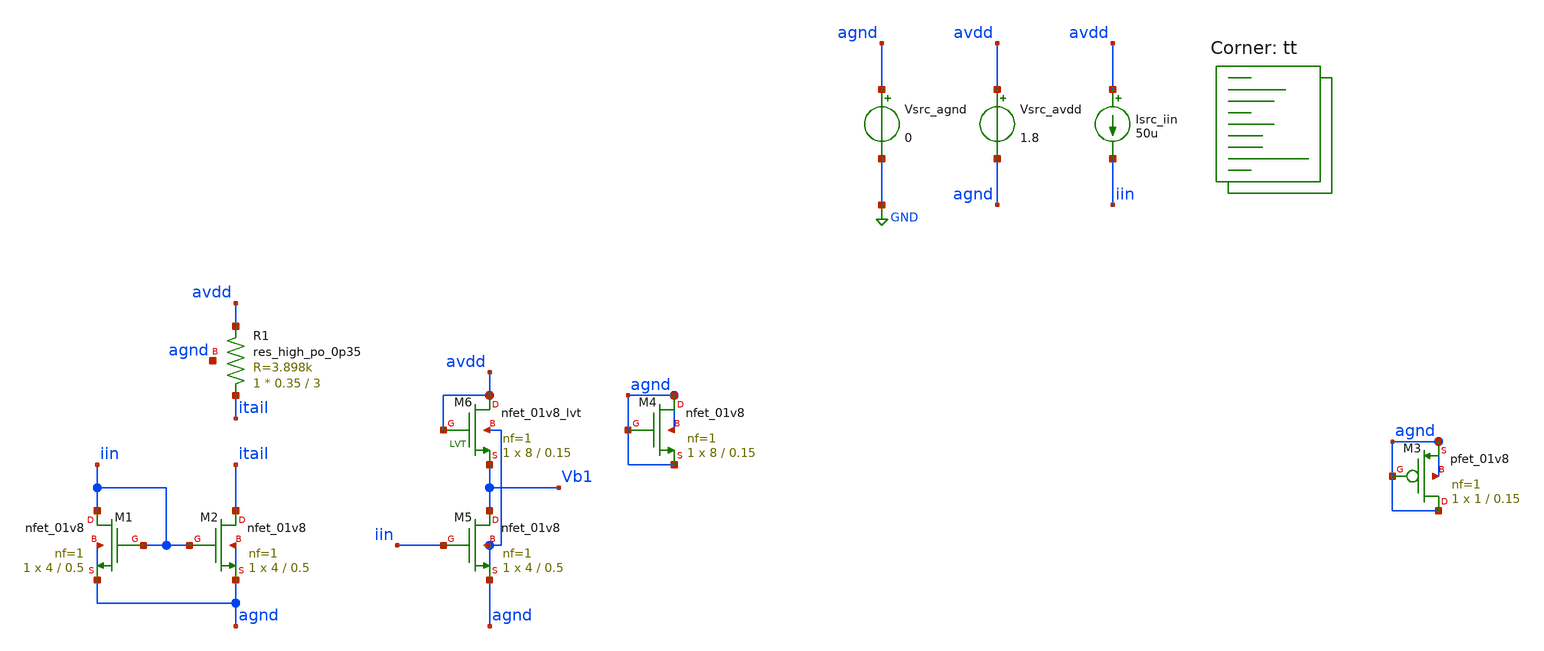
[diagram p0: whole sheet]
** sch_path: AMP/TB_Biases.sch
**.subckt TB_Biases
Vsrc_agnd agnd GND 0
Vsrc_avdd avdd agnd 1.8
Isrc_iin avdd iin 50u
XM1 iin iin agnd agnd sky130_fd_pr__nfet_01v8 L=0.5 W=4 nf=1 ad='int((nf+1)/2) * W/nf * 0.29' as='int((nf+2)/2) * W/nf * 0.29'
+ pd='2*int((nf+1)/2) * (W/nf + 0.29)' ps='2*int((nf+2)/2) * (W/nf + 0.29)' nrd='0.29 / W' nrs='0.29 / W'
+ sa=0 sb=0 sd=0 mult=1 m=1
XM2 itail iin agnd agnd sky130_fd_pr__nfet_01v8 L=0.5 W=4 nf=1 ad='int((nf+1)/2) * W/nf * 0.29' as='int((nf+2)/2) * W/nf * 0.29'
+ pd='2*int((nf+1)/2) * (W/nf + 0.29)' ps='2*int((nf+2)/2) * (W/nf + 0.29)' nrd='0.29 / W' nrs='0.29 / W'
+ sa=0 sb=0 sd=0 mult=1 m=1
XR1 itail avdd agnd sky130_fd_pr__res_high_po_0p35 L=3 mult=1 m=1
XM3 agnd agnd agnd agnd sky130_fd_pr__pfet_01v8 L=0.15 W=1 nf=1 ad='int((nf+1)/2) * W/nf * 0.29' as='int((nf+2)/2) * W/nf * 0.29'
+ pd='2*int((nf+1)/2) * (W/nf + 0.29)' ps='2*int((nf+2)/2) * (W/nf + 0.29)' nrd='0.29 / W' nrs='0.29 / W'
+ sa=0 sb=0 sd=0 mult=1 m=1
XM4 agnd agnd agnd agnd sky130_fd_pr__nfet_01v8 L=0.15 W=8 nf=1 ad='int((nf+1)/2) * W/nf * 0.29' as='int((nf+2)/2) * W/nf * 0.29'
+ pd='2*int((nf+1)/2) * (W/nf + 0.29)' ps='2*int((nf+2)/2) * (W/nf + 0.29)' nrd='0.29 / W' nrs='0.29 / W'
+ sa=0 sb=0 sd=0 mult=1 m=1
XM5 Vb1 iin agnd agnd sky130_fd_pr__nfet_01v8 L=0.5 W=4 nf=1 ad='int((nf+1)/2) * W/nf * 0.29' as='int((nf+2)/2) * W/nf * 0.29'
+ pd='2*int((nf+1)/2) * (W/nf + 0.29)' ps='2*int((nf+2)/2) * (W/nf + 0.29)' nrd='0.29 / W' nrs='0.29 / W'
+ sa=0 sb=0 sd=0 mult=1 m=1
XM6 avdd avdd Vb1 agnd sky130_fd_pr__nfet_01v8_lvt L=0.15 W=8 nf=1 ad='int((nf+1)/2) * W/nf * 0.29' as='int((nf+2)/2) * W/nf * 0.29'
+ pd='2*int((nf+1)/2) * (W/nf + 0.29)' ps='2*int((nf+2)/2) * (W/nf + 0.29)' nrd='0.29 / W' nrs='0.29 / W'
+ sa=0 sb=0 sd=0 mult=1 m=1
**** begin user architecture code

* this option enables mos model bin
* selection based on W/NF instead of W

.option savecurrents

.control
save all
op

* Print newline
echo

* Print stats for each MOSFET
foreach nmos xm1 xm2 xm4 xm5
 * Save stats
 save @m.{$nmos}.msky130_fd_pr__nfet_01v8[gm]
 let vth   = @m.{$nmos}.msky130_fd_pr__nfet_01v8[vth]
 let vgs   = @m.{$nmos}.msky130_fd_pr__nfet_01v8[vgs]
 let vds   = @m.{$nmos}.msky130_fd_pr__nfet_01v8[vds]
 let vdsat = @m.{$nmos}.msky130_fd_pr__nfet_01v8[vdsat]
 let gm    = @m.{$nmos}.msky130_fd_pr__nfet_01v8[gm]
 let gds   = @m.{$nmos}.msky130_fd_pr__nfet_01v8[gds]


 * Print stats
 echo Stats for $nmos:
 print vth
 print vgs
 print vds
 print vdsat
 print gm
 print gds

 * Print newline
 echo
end

foreach nmos_lvt xm6
 * Save stats
 save @m.{$nmos_lvt}.msky130_fd_pr__nfet_01v8_lvt[gm]
 let vth   = @m.{$nmos_lvt}.msky130_fd_pr__nfet_01v8_lvt[vth]
 let vgs   = @m.{$nmos_lvt}.msky130_fd_pr__nfet_01v8_lvt[vgs]
 let vds   = @m.{$nmos_lvt}.msky130_fd_pr__nfet_01v8_lvt[vds]
 let vdsat = @m.{$nmos_lvt}.msky130_fd_pr__nfet_01v8_lvt[vdsat]
 let gm    = @m.{$nmos_lvt}.msky130_fd_pr__nfet_01v8_lvt[gm]
 let gds   = @m.{$nmos_lvt}.msky130_fd_pr__nfet_01v8_lvt[gds]


 * Print stats
 echo Stats for $nmos_lvt:
 print vth
 print vgs
 print vds
 print vdsat
 print gm
 print gds

 * Print newline
 echo
end

foreach pmos xm3
 * Save stats
 save @m.{$pmos}.msky130_fd_pr__nfet_01v8[gm]
 let vth   = @m.{$pmos}.msky130_fd_pr__pfet_01v8[vth]
 let vgs   = @m.{$pmos}.msky130_fd_pr__pfet_01v8[vgs]
 let vds   = @m.{$pmos}.msky130_fd_pr__pfet_01v8[vds]
 let vdsat = @m.{$pmos}.msky130_fd_pr__pfet_01v8[vdsat]
 let gm    = @m.{$pmos}.msky130_fd_pr__pfet_01v8[gm]
 let gds   = @m.{$pmos}.msky130_fd_pr__pfet_01v8[gds]

 * Print stats
 echo Stats for $pmos:
 print vth
 print vgs
 print vds
 print vdsat
 print gm
 print gds

 * Print newline
 echo
end

* Print region of operation
echo Regions of Operation:
foreach nmos xm1 xm2 xm4 xm5
 * Save stats
 let vds = @m.{$nmos}.msky130_fd_pr__nfet_01v8[vds]
 let vgs = @m.{$nmos}.msky130_fd_pr__nfet_01v8[vgs]
 let vth = @m.{$nmos}.msky130_fd_pr__nfet_01v8[vth]

 * Check and print regions
 if (vgs <= vth)
  echo $nmos: N Cutoff
  print vgs
  print vth
 end
 if (vgs > vth) & (vds <= (vgs - vth))
  echo $nmos: N Triode
  print vgs
  print vth
  print vds
 end
 if (vgs > vth) & (vds > (vgs - vth))
  echo $nmos: N Saturation
 end
end

* Print region of operation
foreach nmos_lvt xm6
 * Save stats
 let vds = @m.{$nmos_lvt}.msky130_fd_pr__nfet_01v8_lvt[vds]
 let vgs = @m.{$nmos_lvt}.msky130_fd_pr__nfet_01v8_lvt[vgs]
 let vth = @m.{$nmos_lvt}.msky130_fd_pr__nfet_01v8_lvt[vth]

 * Check and print regions
 if (vgs <= vth)
  echo $nmos_lvt: N Cutoff
  print vgs
  print vth
 end
 if (vgs > vth) & (vds <= (vgs - vth))
  echo $nmos_lvt: N Triode
  print vgs
  print vth
  print vds
 end
 if (vgs > vth) & (vds > (vgs - vth))
  echo $nmos_lvt: N Saturation
 end
end

foreach pmos xm3
 * Save stats
 let vds = @m.{$pmos}.msky130_fd_pr__pfet_01v8[vds]
 let vgs = @m.{$pmos}.msky130_fd_pr__pfet_01v8[vgs]
 let vth = @m.{$pmos}.msky130_fd_pr__pfet_01v8[vth]

 * Check and print regions
 if (abs(vgs) <= abs(vth))
  echo $pmos: P Cutoff
  print vgs
  print vth
 end
 if (abs(vgs) > abs(vth)) & (abs(vds) <= (abs(vgs) - abs(vth)))
  echo $pmos: P Triode
  print vgs
  print vth
  print vds
 end
 if (abs(vgs) > abs(vth)) & (abs(vds) > (abs(vgs) - abs(vth)))
  echo $pmos: P Saturation
 end
end

* Print newline
echo

write TB_Biases.raw

.endc


.lib $::SKYWATER_MODELS/sky130.lib.spice tt
**** end user architecture code
**.ends
.GLOBAL GND
.end
